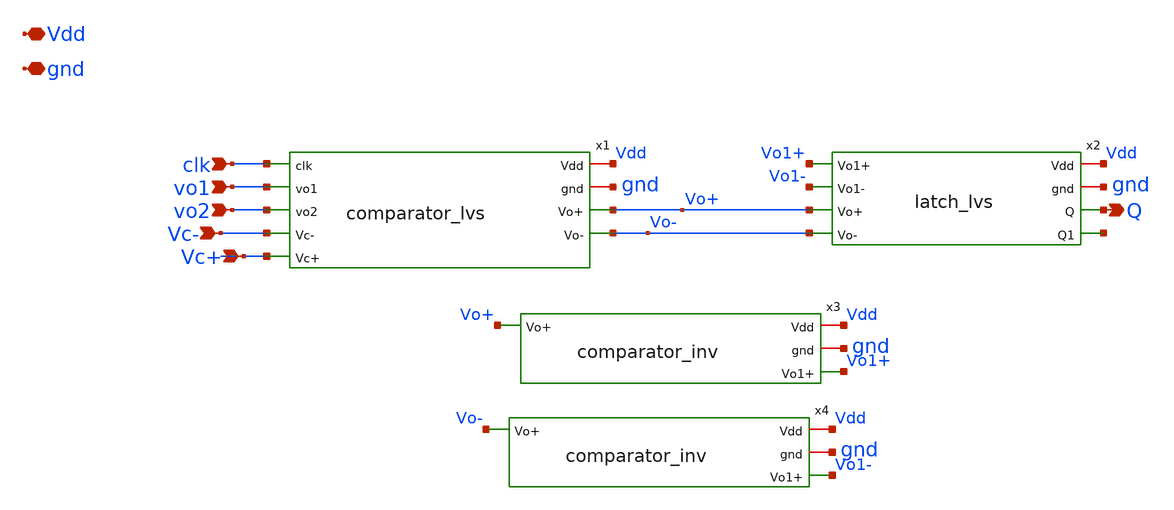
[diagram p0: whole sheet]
** sch_path: xschem/charge_pumps2/sense_amp_comparator.sch
**.subckt sense_amp_comparator gnd Vdd clk vo1 vo2 Vc- Vc+ Q
*.iopin gnd
*.iopin Vdd
*.ipin clk
*.ipin vo1
*.ipin vo2
*.ipin Vc-
*.ipin Vc+
*.opin Q
x1 Vdd gnd clk vo1 vo2 Vc- Vc+ Vo+ Vo- comparator_lvs
x2 Vdd gnd Q net1 Vo1+ Vo1- Vo+ Vo- latch_lvs
x3 Vdd gnd Vo+ Vo1+ comparator_inv
x4 Vdd gnd Vo- Vo1- comparator_inv
**.ends
.end
